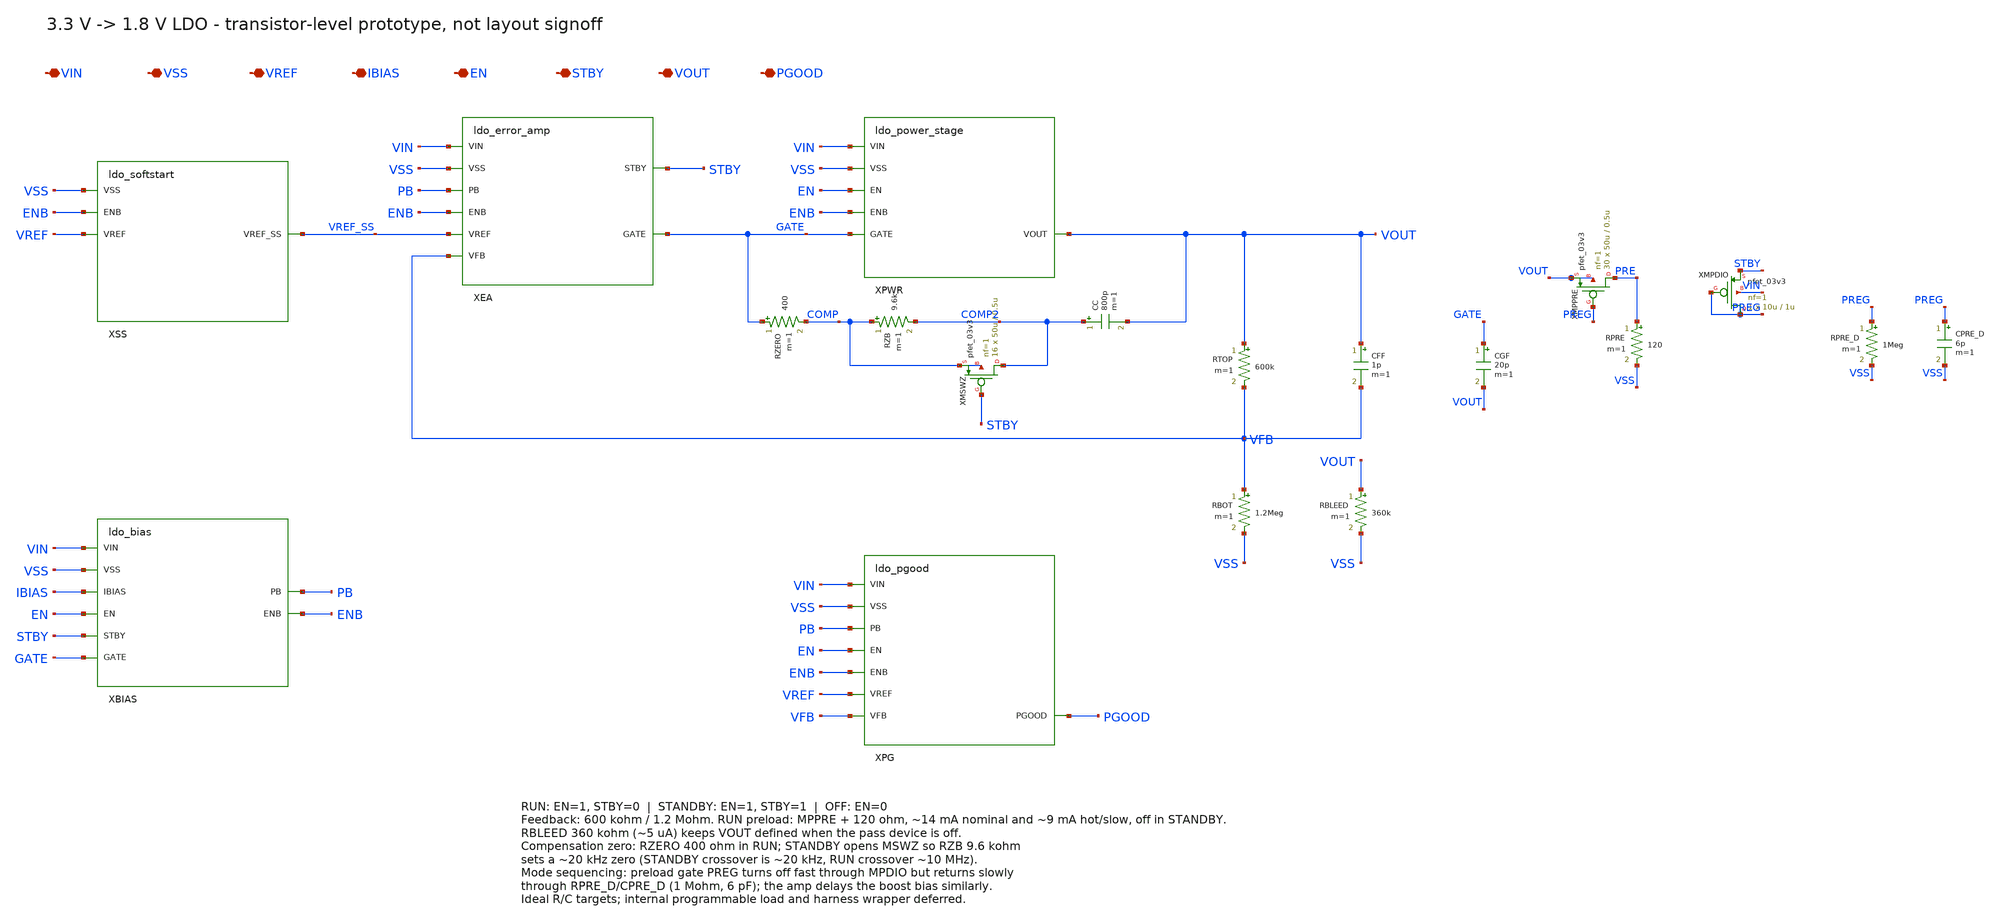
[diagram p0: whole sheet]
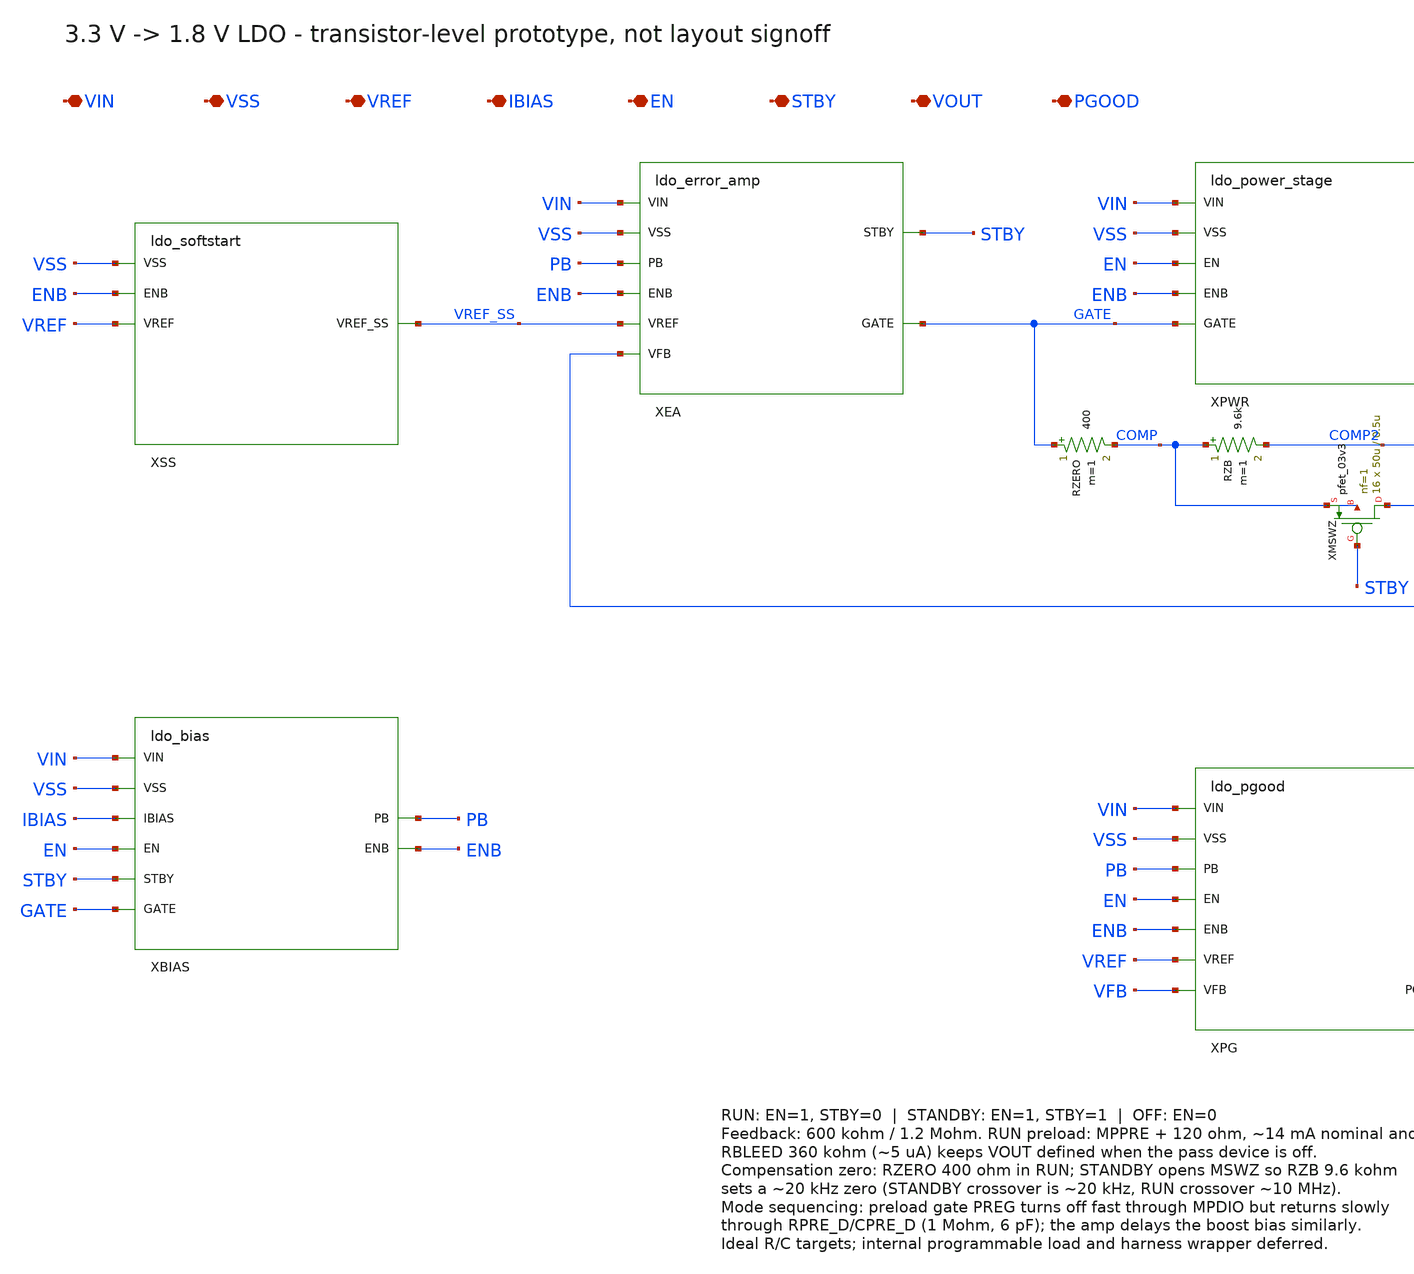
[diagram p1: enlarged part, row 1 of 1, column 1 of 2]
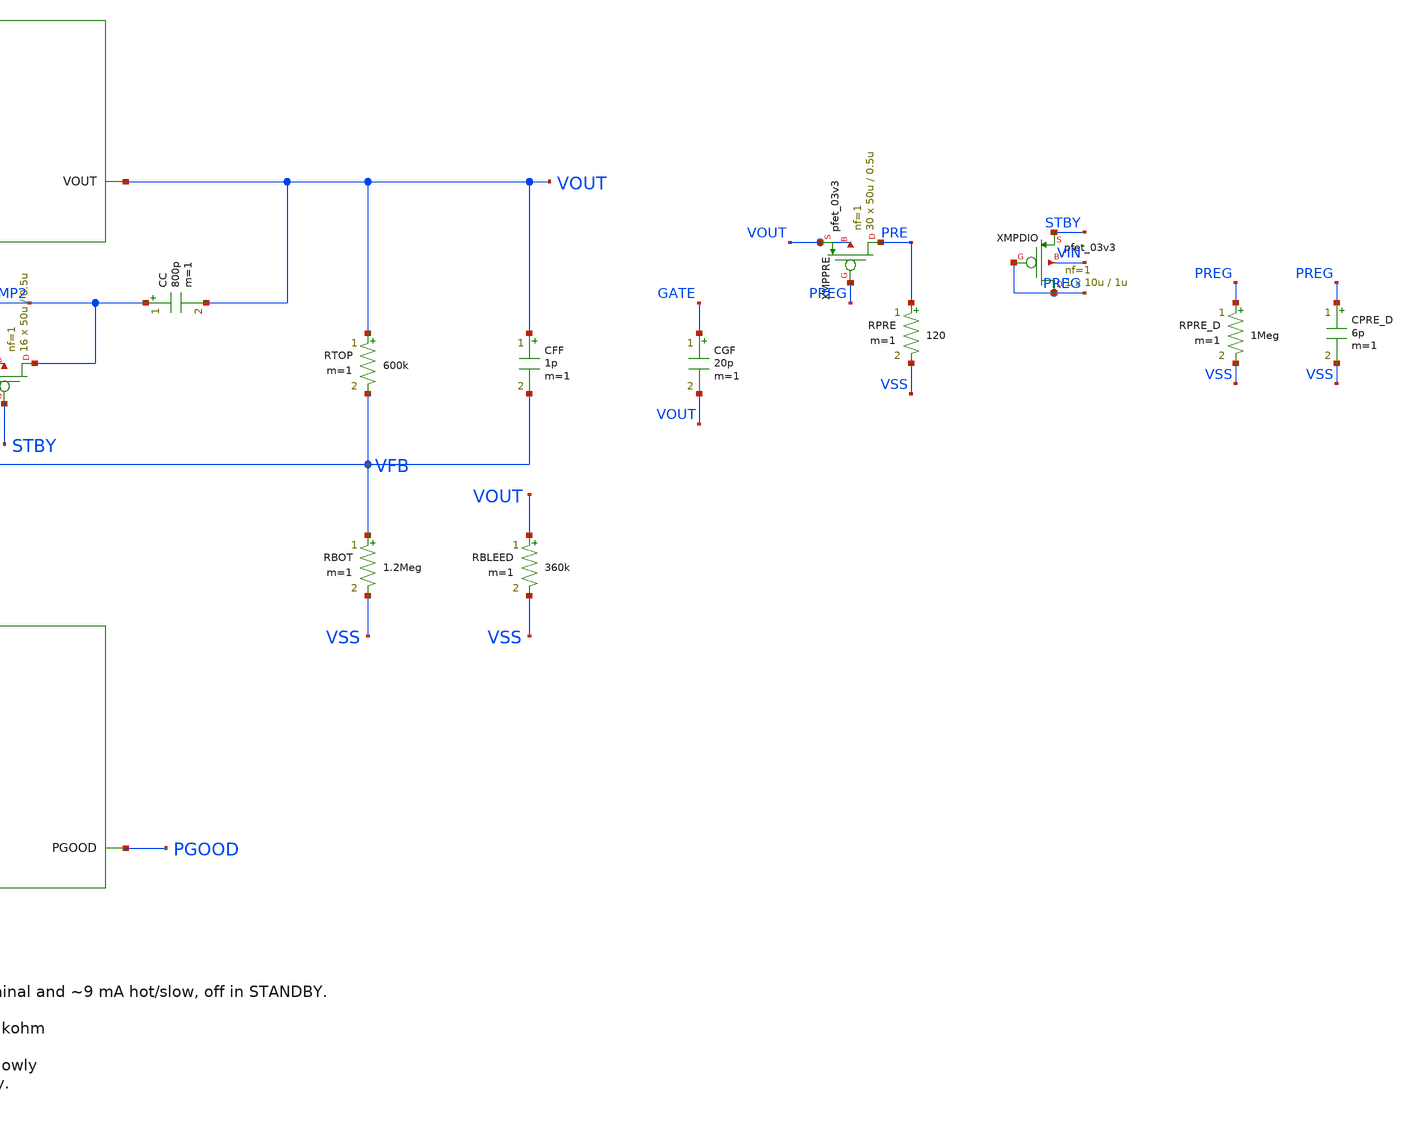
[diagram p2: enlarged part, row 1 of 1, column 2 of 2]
** sch_path: schematics/ldo_top.sch
**.subckt ldo_top VIN VSS VREF IBIAS EN STBY VOUT PGOOD
*.iopin VIN
*.iopin VSS
*.iopin VREF
*.iopin IBIAS
*.iopin EN
*.iopin STBY
*.iopin VOUT
*.iopin PGOOD
XSS VSS ENB VREF VREF_SS ldo_softstart
XEA VIN VSS PB ENB STBY VREF_SS VFB GATE ldo_error_amp
XPWR VIN VSS EN ENB GATE VOUT ldo_power_stage
XBIAS VIN VSS IBIAS EN STBY GATE ENB PB ldo_bias
XPG VIN VSS PB EN ENB VREF VFB PGOOD ldo_pgood
RTOP VOUT VFB 600k m=1
RBOT VFB VSS 1.2Meg m=1
CFF VOUT VFB 1p m=1
RZERO GATE COMP 400 m=1
RZB COMP COMP2 9.6k m=1
XMSWZ COMP2 STBY COMP COMP pfet_03v3 L=0.5u W=50u nf=1 ad='int((nf+1)/2)*W/nf*0.18u' as='int((nf+2)/2)*W/nf*0.18u'
+ pd='2*int((nf+1)/2)*(W/nf+0.18u)' ps='2*int((nf+2)/2)*(W/nf+0.18u)' nrd='0.18u/W' nrs='0.18u/W' sa=0
+ sb=0 sd=0 m=16 par=16
CC COMP2 VOUT 800p m=1
RBLEED VOUT VSS 360k m=1
CGF GATE VOUT 20p m=1
XMPPRE PRE PREG VOUT VOUT pfet_03v3 L=0.5u W=50u nf=1 ad='int((nf+1)/2)*W/nf*0.18u' as='int((nf+2)/2)*W/nf*0.18u'
+ pd='2*int((nf+1)/2)*(W/nf+0.18u)' ps='2*int((nf+2)/2)*(W/nf+0.18u)' nrd='0.18u/W' nrs='0.18u/W' sa=0
+ sb=0 sd=0 m=30 par=30
RPRE PRE VSS 120 m=1
XMPDIO PREG PREG STBY VIN pfet_03v3 L=1u W=10u nf=1 ad='int((nf+1)/2)*W/nf*0.18u' as='int((nf+2)/2)*W/nf*0.18u'
+ pd='2*int((nf+1)/2)*(W/nf+0.18u)' ps='2*int((nf+2)/2)*(W/nf+0.18u)' nrd='0.18u/W' nrs='0.18u/W' sa=0
+ sb=0 sd=0 m=1 par=1
RPRE_D PREG VSS 1Meg m=1
CPRE_D PREG VSS 6p m=1
**.ends
.end
